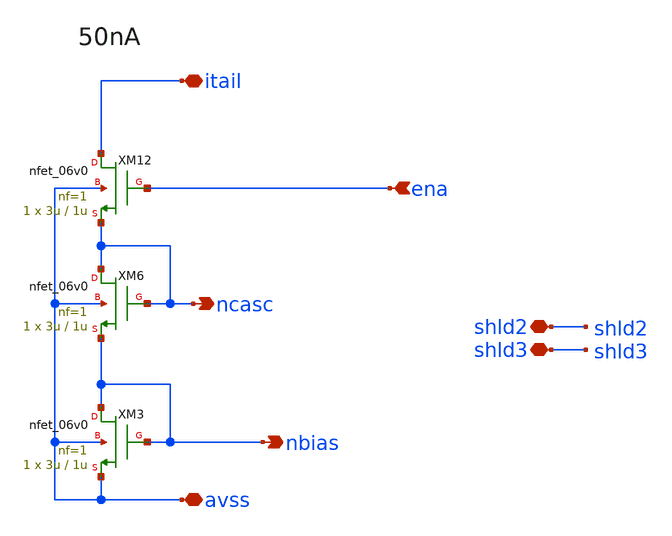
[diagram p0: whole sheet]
** sch_path: xschem/bias_nset.sch
**.subckt bias_nset avss ena itail nbias ncasc shld2 shld3
*.iopin avss
*.ipin ena
*.iopin itail
*.opin nbias
*.opin ncasc
*.iopin shld2
*.iopin shld3
XM3 nbias nbias avss avss nfet_06v0 L=1u W=3u nf=1 ad='int((nf+1)/2) * W/nf * 0.18u' as='int((nf+2)/2) * W/nf * 0.18u'
+ pd='2*int((nf+1)/2) * (W/nf + 0.18u)' ps='2*int((nf+2)/2) * (W/nf + 0.18u)' nrd='0.18u / W' nrs='0.18u / W'
+ sa=0 sb=0 sd=0 m=1 par=1
XM6 ncasc ncasc nbias avss nfet_06v0 L=1u W=3u nf=1 ad='int((nf+1)/2) * W/nf * 0.18u' as='int((nf+2)/2) * W/nf * 0.18u'
+ pd='2*int((nf+1)/2) * (W/nf + 0.18u)' ps='2*int((nf+2)/2) * (W/nf + 0.18u)' nrd='0.18u / W' nrs='0.18u / W'
+ sa=0 sb=0 sd=0 m=1 par=1
XM12 itail ena ncasc avss nfet_06v0 L=1u W=3u nf=1 ad='int((nf+1)/2) * W/nf * 0.18u' as='int((nf+2)/2) * W/nf * 0.18u'
+ pd='2*int((nf+1)/2) * (W/nf + 0.18u)' ps='2*int((nf+2)/2) * (W/nf + 0.18u)' nrd='0.18u / W' nrs='0.18u / W'
+ sa=0 sb=0 sd=0 m=1 par=1
**.ends
.end
